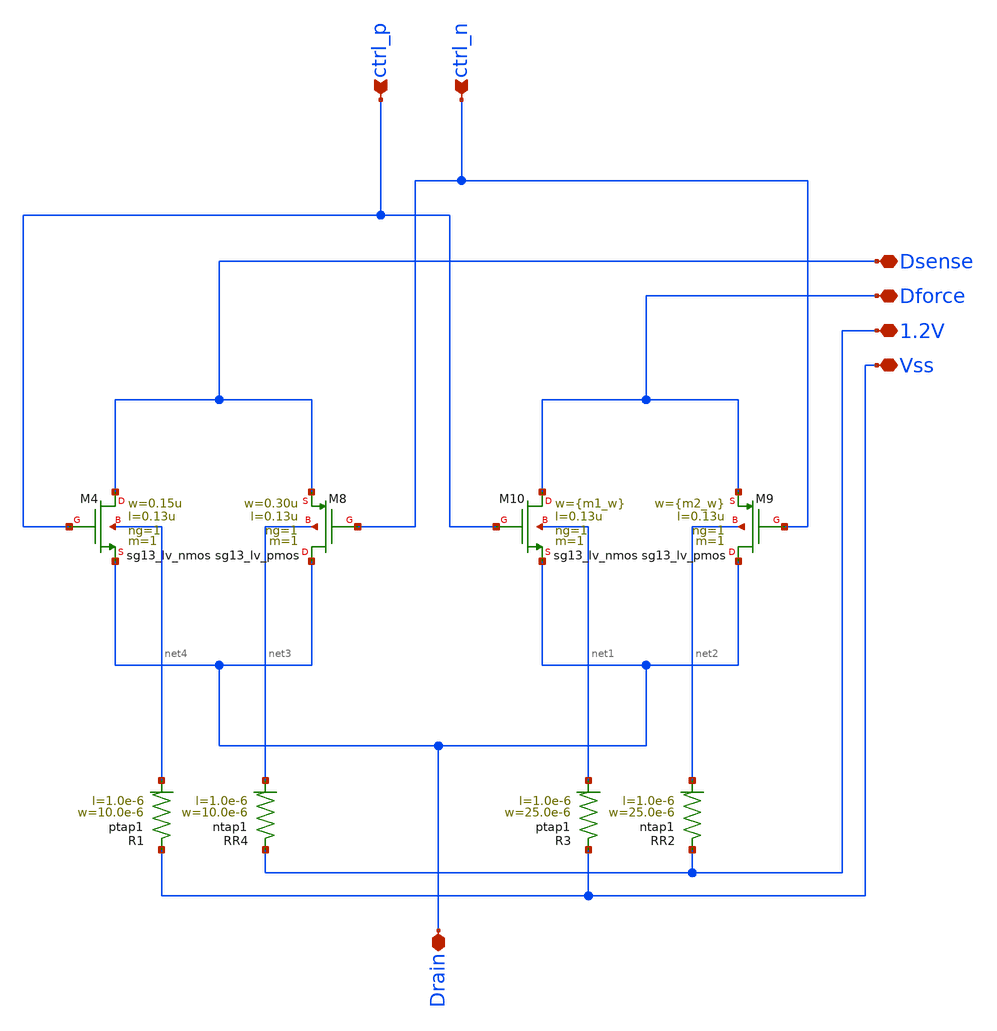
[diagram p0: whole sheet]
** sch_path: design_data/xschem/Drain_Line.sch
**.subckt Drain_Line Vss ctrl_n 1.2V Dsense Drain Dforce ctrl_p
*.iopin Vss
*.ipin ctrl_n
*.iopin 1.2V
*.iopin Dsense
*.iopin Drain
*.iopin Dforce
*.ipin ctrl_p
XM4 Dsense ctrl_p Drain net4 sg13_lv_nmos w=0.15u l=0.13u ng=1 m=1 mm_ok=1
XM8 Drain ctrl_n Dsense net3 sg13_lv_pmos w=0.30u l=0.13u ng=1 m=1 mm_ok=1
XM9 Drain ctrl_n Dforce net2 sg13_lv_pmos w={m2_w} l=0.13u ng=1 m=1 mm_ok=1
XM10 Dforce ctrl_p Drain net1 sg13_lv_nmos w={m1_w} l=0.13u ng=1 m=1 mm_ok=1
XR1 Vss net4 ptap1 R=30.62 w=10.0e-6 l=1.0e-6
XR2 1.2V net2 ntap1 R=12.73 w=25.0e-6 l=1.0e-6
XR3 Vss net1 ptap1 R=12.73 w=25.0e-6 l=1.0e-6
XR4 1.2V net3 ntap1 R=30.62 w=10.0e-6 l=1.0e-6
**.ends
.end
